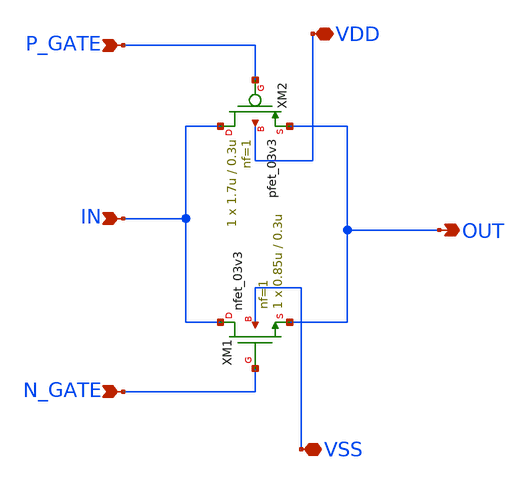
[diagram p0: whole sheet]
** sch_path: designs/cells/sdffrnq/sch/mux_tg.sch
**.subckt mux_tg VDD VSS OUT IN P_GATE N_GATE
*.iopin VDD
*.iopin VSS
*.opin OUT
*.ipin IN
*.ipin P_GATE
*.ipin N_GATE
XM1 IN N_GATE OUT VSS nfet_03v3 L=0.3u W=0.85u nf=1 ad='int((nf+1)/2) * W/nf * 0.18u' as='int((nf+2)/2) * W/nf * 0.18u'
+ pd='2*int((nf+1)/2) * (W/nf + 0.18u)' ps='2*int((nf+2)/2) * (W/nf + 0.18u)' nrd='0.18u / W' nrs='0.18u / W'
+ sa=0 sb=0 sd=0 m=1
XM2 IN P_GATE OUT VDD pfet_03v3 L=0.3u W=1.7u nf=1 ad='int((nf+1)/2) * W/nf * 0.18u' as='int((nf+2)/2) * W/nf * 0.18u'
+ pd='2*int((nf+1)/2) * (W/nf + 0.18u)' ps='2*int((nf+2)/2) * (W/nf + 0.18u)' nrd='0.18u / W' nrs='0.18u / W'
+ sa=0 sb=0 sd=0 m=1
**.ends
.end
